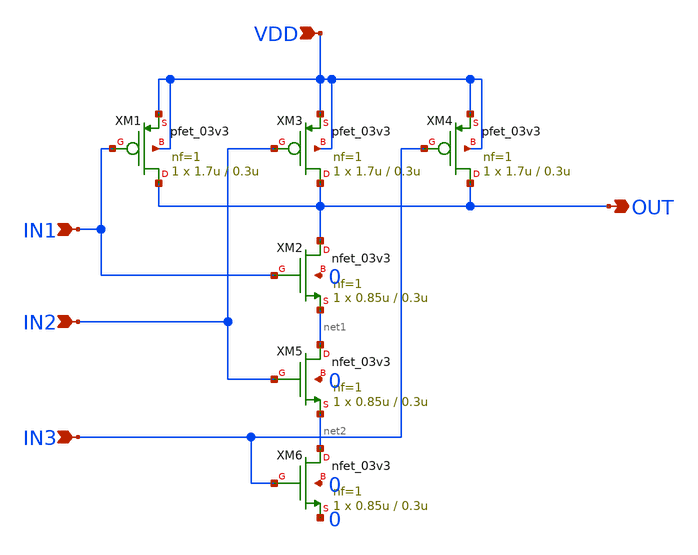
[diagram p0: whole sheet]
** sch_path: chipathon_2023/initial_notebooks_2023/accepted_notebooks/Current-Steering-DAC/DAC/NAND3_1.sch
**.subckt NAND3_1 VDD IN1 IN2 IN3 OUT
*.ipin VDD
*.ipin IN1
*.ipin IN2
*.ipin IN3
*.opin OUT
XM1 OUT IN1 VDD VDD pfet_03v3 L=0.3u W=1.7u nf=1 ad='int((nf+1)/2) * W/nf * 0.18u' as='int((nf+2)/2) * W/nf * 0.18u'
+ pd='2*int((nf+1)/2) * (W/nf + 0.18u)' ps='2*int((nf+2)/2) * (W/nf + 0.18u)' nrd='0.18u / W' nrs='0.18u / W'
+ sa=0 sb=0 sd=0 m=1
XM2 OUT IN1 net1 0 nfet_03v3 L=0.3u W=0.85u nf=1 ad='int((nf+1)/2) * W/nf * 0.18u' as='int((nf+2)/2) * W/nf * 0.18u'
+ pd='2*int((nf+1)/2) * (W/nf + 0.18u)' ps='2*int((nf+2)/2) * (W/nf + 0.18u)' nrd='0.18u / W' nrs='0.18u / W'
+ sa=0 sb=0 sd=0 m=1
XM3 OUT IN2 VDD VDD pfet_03v3 L=0.3u W=1.7u nf=1 ad='int((nf+1)/2) * W/nf * 0.18u' as='int((nf+2)/2) * W/nf * 0.18u'
+ pd='2*int((nf+1)/2) * (W/nf + 0.18u)' ps='2*int((nf+2)/2) * (W/nf + 0.18u)' nrd='0.18u / W' nrs='0.18u / W'
+ sa=0 sb=0 sd=0 m=1
XM4 OUT IN3 VDD VDD pfet_03v3 L=0.3u W=1.7u nf=1 ad='int((nf+1)/2) * W/nf * 0.18u' as='int((nf+2)/2) * W/nf * 0.18u'
+ pd='2*int((nf+1)/2) * (W/nf + 0.18u)' ps='2*int((nf+2)/2) * (W/nf + 0.18u)' nrd='0.18u / W' nrs='0.18u / W'
+ sa=0 sb=0 sd=0 m=1
XM5 net1 IN2 net2 0 nfet_03v3 L=0.3u W=0.85u nf=1 ad='int((nf+1)/2) * W/nf * 0.18u' as='int((nf+2)/2) * W/nf * 0.18u'
+ pd='2*int((nf+1)/2) * (W/nf + 0.18u)' ps='2*int((nf+2)/2) * (W/nf + 0.18u)' nrd='0.18u / W' nrs='0.18u / W'
+ sa=0 sb=0 sd=0 m=1
XM6 net2 IN3 0 0 nfet_03v3 L=0.3u W=0.85u nf=1 ad='int((nf+1)/2) * W/nf * 0.18u' as='int((nf+2)/2) * W/nf * 0.18u'
+ pd='2*int((nf+1)/2) * (W/nf + 0.18u)' ps='2*int((nf+2)/2) * (W/nf + 0.18u)' nrd='0.18u / W' nrs='0.18u / W'
+ sa=0 sb=0 sd=0 m=1
**.ends
.end
